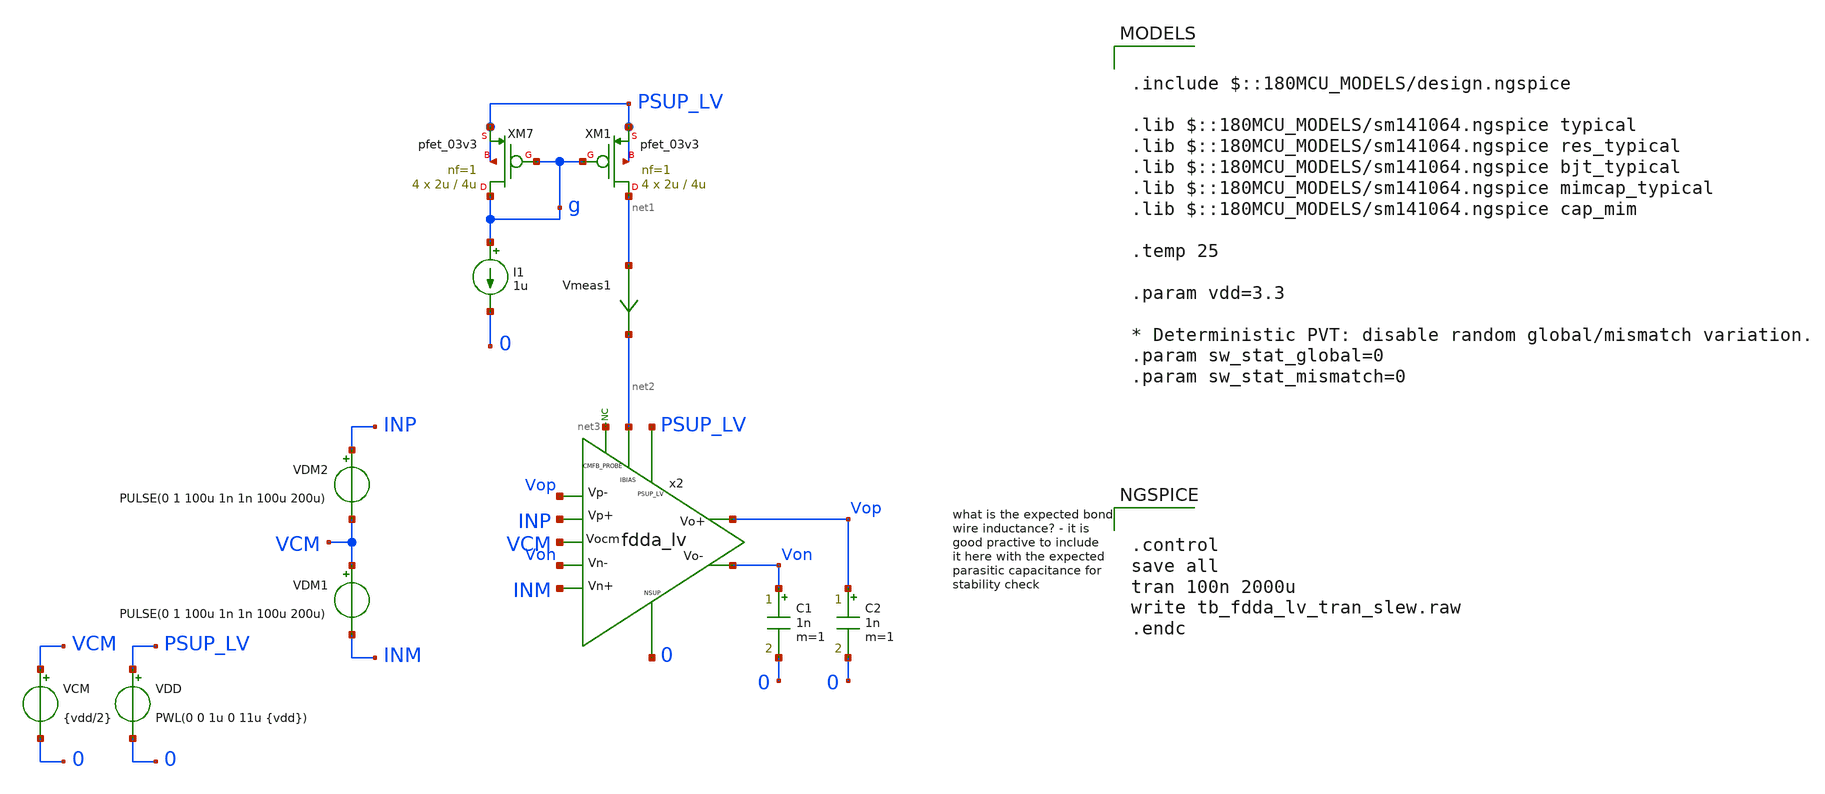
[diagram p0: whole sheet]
** sch_path: xschem/blocks/fdda_lv/tb_fdda_lv_tran_slew.sch
**.subckt tb_fdda_lv_tran_slew
C1 Von 0 1n m=1
x2 PSUP_LV Vop Von INM INP Vop Von net2 0 net3 VCM fdda_lv
VDD PSUP_LV 0 PWL(0 0 1u 0 11u {vdd})
C2 Vop 0 1n m=1
VCM VCM 0 {vdd/2}
VDM2 INP VCM PULSE(0 1 100u 1n 1n 100u 200u)
VDM1 VCM INM PULSE(0 1 100u 1n 1n 100u 200u)
* noconn #net3
XM7 g g PSUP_LV PSUP_LV pfet_03v3 L=4u W=2u nf=1 ad='int((nf+1)/2) * W/nf * 0.18u' as='int((nf+2)/2) * W/nf * 0.18u'
+ pd='2*int((nf+1)/2) * (W/nf + 0.18u)' ps='2*int((nf+2)/2) * (W/nf + 0.18u)' nrd='0.18u / W' nrs='0.18u / W'
+ sa=0 sb=0 sd=0 m=4
XM1 net1 g PSUP_LV PSUP_LV pfet_03v3 L=4u W=2u nf=1 ad='int((nf+1)/2) * W/nf * 0.18u' as='int((nf+2)/2) * W/nf * 0.18u'
+ pd='2*int((nf+1)/2) * (W/nf + 0.18u)' ps='2*int((nf+2)/2) * (W/nf + 0.18u)' nrd='0.18u / W' nrs='0.18u / W'
+ sa=0 sb=0 sd=0 m=4
I1 g 0 1u
Vmeas1 net1 net2 0
.save i(vmeas1)
**** begin user architecture code

.include $::180MCU_MODELS/design.ngspice

.lib $::180MCU_MODELS/sm141064.ngspice typical
.lib $::180MCU_MODELS/sm141064.ngspice res_typical
.lib $::180MCU_MODELS/sm141064.ngspice bjt_typical
.lib $::180MCU_MODELS/sm141064.ngspice mimcap_typical
.lib $::180MCU_MODELS/sm141064.ngspice cap_mim

.temp 25

.param vdd=3.3

* Deterministic PVT: disable random global/mismatch variation.
.param sw_stat_global=0
.param sw_stat_mismatch=0



.control
save all
tran 100n 2000u
write tb_fdda_lv_tran_slew.raw
.endc


**** end user architecture code
**.ends
.end
